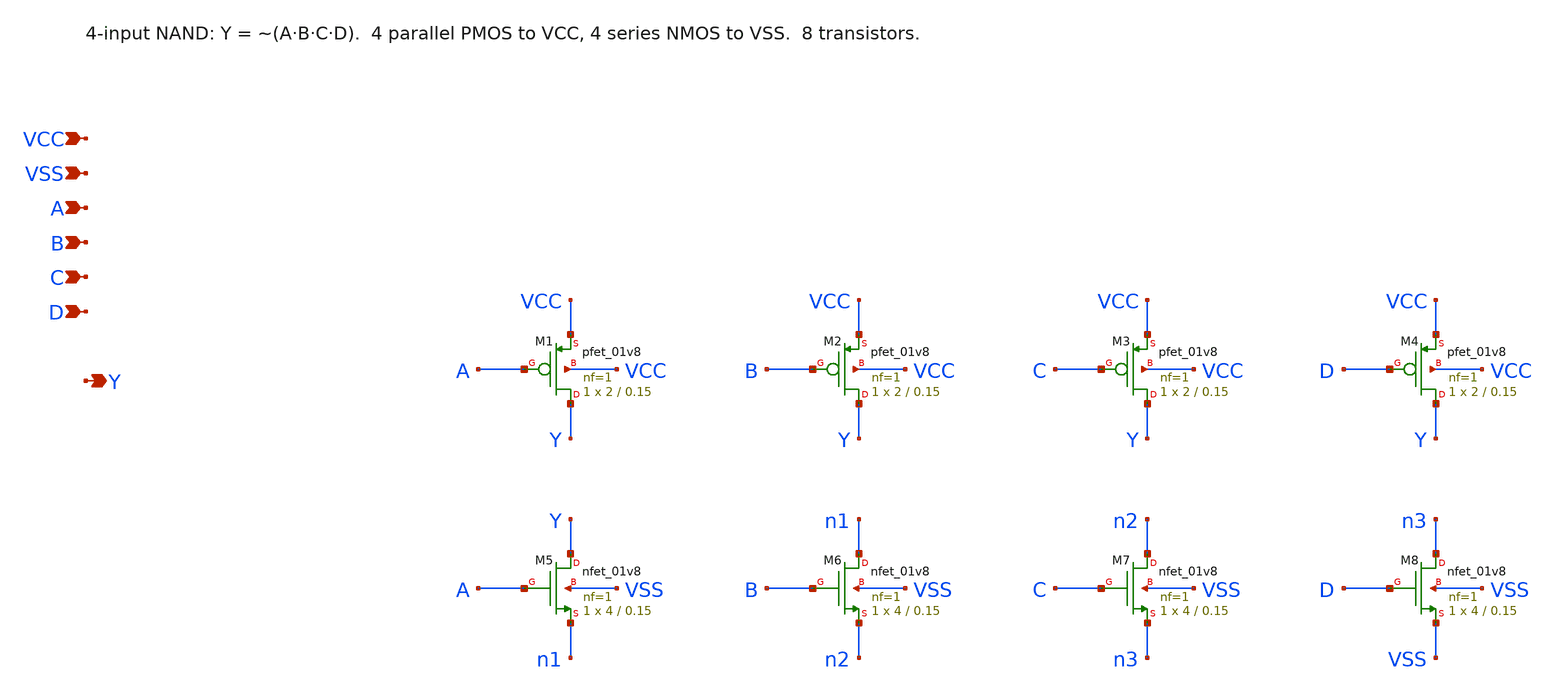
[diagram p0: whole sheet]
** sch_path: nand4.sch
**.subckt nand4 VCC VSS A B C D Y
*.ipin VCC
*.ipin VSS
*.ipin A
*.ipin B
*.ipin C
*.ipin D
*.opin Y
XM1 Y A VCC VCC sky130_fd_pr__pfet_01v8 L=0.15 W=2 nf=1 ad='int((nf+1)/2) * W/nf * 0.29' as='int((nf+2)/2) * W/nf * 0.29'
+ pd='2*int((nf+1)/2) * (W/nf + 0.29)' ps='2*int((nf+2)/2) * (W/nf + 0.29)' nrd='0.29 / W' nrs='0.29 / W'
+ sa=0 sb=0 sd=0 mult=1 m=1
XM2 Y B VCC VCC sky130_fd_pr__pfet_01v8 L=0.15 W=2 nf=1 ad='int((nf+1)/2) * W/nf * 0.29' as='int((nf+2)/2) * W/nf * 0.29'
+ pd='2*int((nf+1)/2) * (W/nf + 0.29)' ps='2*int((nf+2)/2) * (W/nf + 0.29)' nrd='0.29 / W' nrs='0.29 / W'
+ sa=0 sb=0 sd=0 mult=1 m=1
XM3 Y C VCC VCC sky130_fd_pr__pfet_01v8 L=0.15 W=2 nf=1 ad='int((nf+1)/2) * W/nf * 0.29' as='int((nf+2)/2) * W/nf * 0.29'
+ pd='2*int((nf+1)/2) * (W/nf + 0.29)' ps='2*int((nf+2)/2) * (W/nf + 0.29)' nrd='0.29 / W' nrs='0.29 / W'
+ sa=0 sb=0 sd=0 mult=1 m=1
XM4 Y D VCC VCC sky130_fd_pr__pfet_01v8 L=0.15 W=2 nf=1 ad='int((nf+1)/2) * W/nf * 0.29' as='int((nf+2)/2) * W/nf * 0.29'
+ pd='2*int((nf+1)/2) * (W/nf + 0.29)' ps='2*int((nf+2)/2) * (W/nf + 0.29)' nrd='0.29 / W' nrs='0.29 / W'
+ sa=0 sb=0 sd=0 mult=1 m=1
XM5 Y A n1 VSS sky130_fd_pr__nfet_01v8 L=0.15 W=4 nf=1 ad='int((nf+1)/2) * W/nf * 0.29' as='int((nf+2)/2) * W/nf * 0.29'
+ pd='2*int((nf+1)/2) * (W/nf + 0.29)' ps='2*int((nf+2)/2) * (W/nf + 0.29)' nrd='0.29 / W' nrs='0.29 / W'
+ sa=0 sb=0 sd=0 mult=1 m=1
XM6 n1 B n2 VSS sky130_fd_pr__nfet_01v8 L=0.15 W=4 nf=1 ad='int((nf+1)/2) * W/nf * 0.29' as='int((nf+2)/2) * W/nf * 0.29'
+ pd='2*int((nf+1)/2) * (W/nf + 0.29)' ps='2*int((nf+2)/2) * (W/nf + 0.29)' nrd='0.29 / W' nrs='0.29 / W'
+ sa=0 sb=0 sd=0 mult=1 m=1
XM7 n2 C n3 VSS sky130_fd_pr__nfet_01v8 L=0.15 W=4 nf=1 ad='int((nf+1)/2) * W/nf * 0.29' as='int((nf+2)/2) * W/nf * 0.29'
+ pd='2*int((nf+1)/2) * (W/nf + 0.29)' ps='2*int((nf+2)/2) * (W/nf + 0.29)' nrd='0.29 / W' nrs='0.29 / W'
+ sa=0 sb=0 sd=0 mult=1 m=1
XM8 n3 D VSS VSS sky130_fd_pr__nfet_01v8 L=0.15 W=4 nf=1 ad='int((nf+1)/2) * W/nf * 0.29' as='int((nf+2)/2) * W/nf * 0.29'
+ pd='2*int((nf+1)/2) * (W/nf + 0.29)' ps='2*int((nf+2)/2) * (W/nf + 0.29)' nrd='0.29 / W' nrs='0.29 / W'
+ sa=0 sb=0 sd=0 mult=1 m=1
**.ends
.end
